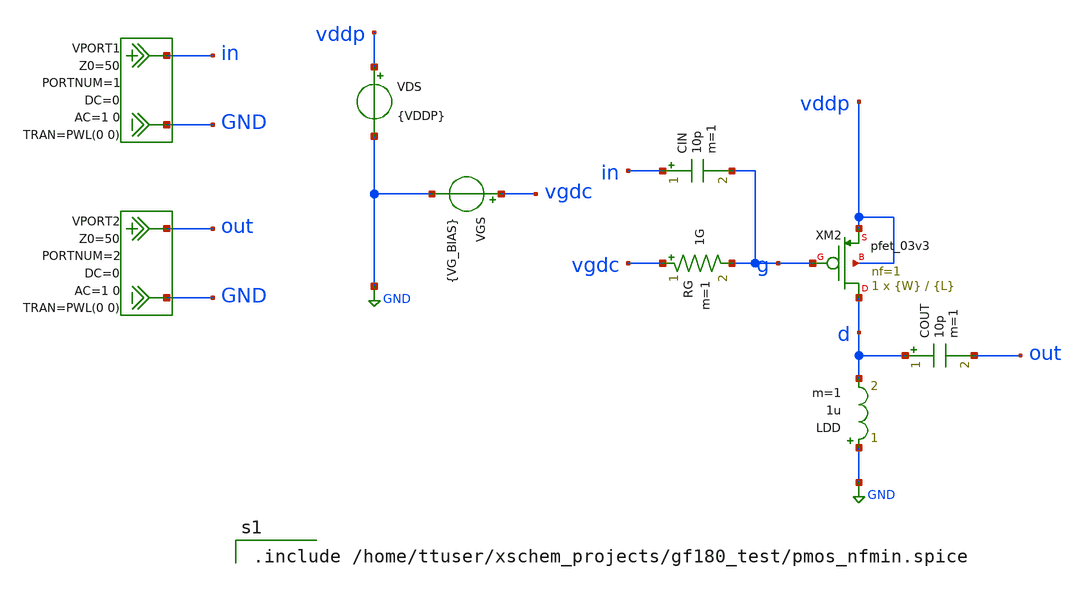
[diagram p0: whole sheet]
** sch_path: simulations/nfmin_sweeps/nfmin_jd_pmos.sch
**.subckt nfmin_jd_pmos
VGS vgdc GND {VG_BIAS}
VDS vddp GND {VDDP}
LDD GND d 1u m=1
RG vgdc g 1G m=1
COUT d out 10p m=1
VPORT1 in GND DC 0 AC 1 0 portnum 1 z0 50 PWL(0 0)
VPORT2 out GND DC 0 AC 1 0 portnum 2 z0 50 PWL(0 0)
CIN in g 10p m=1
XM2 d g vddp vddp pfet_03v3 L={L} W={W} nf=1 ad='int((nf+1)/2) * W/nf * 0.18u' as='int((nf+2)/2) * W/nf * 0.18u'
+ pd='2*int((nf+1)/2) * (W/nf + 0.18u)' ps='2*int((nf+2)/2) * (W/nf + 0.18u)' nrd='0.18u / W' nrs='0.18u / W'
+ sa=0 sb=0 sd=0 m=1
**** begin user architecture code

.include /home/ttuser/xschem_projects/gf180_test/pmos_nfmin.spice

**** end user architecture code
**.ends
.GLOBAL GND
.end
